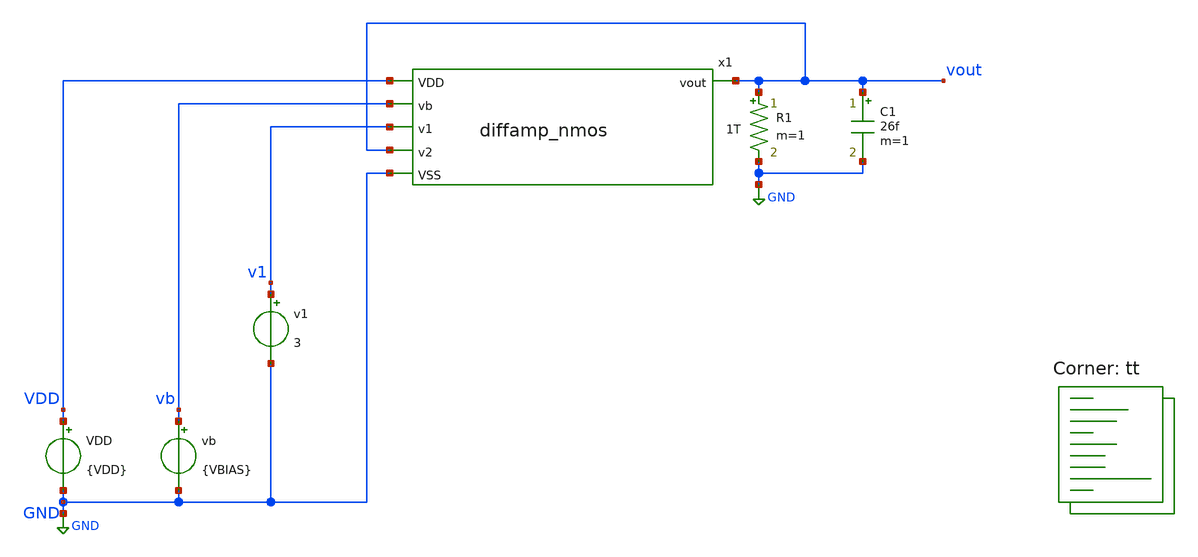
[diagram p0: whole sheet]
** sch_path: xschem/test_diffamp_nmos_load.sch
**.subckt test_diffamp_nmos_load
VDD VDD GND {VDD}
vb vb GND {VBIAS}
v1 v1 GND 3
R1 vout GND 1T m=1
x1 v1 vout GND VDD vb vout diffamp_nmos
C1 vout GND 26f m=1
**** begin user architecture code
.lib $::SKYWATER_MODELS/sky130.lib.spice tt



.options reltol=0.0001 abstol=10e-15
*.include diffamp_nmos.spice
.param VDD=6
.param VSS=0
.param VBIAS=1.2
.options savecurrents
* .options reltol=0.01 abstol=10e-12
.control
  save all
  op
  remzerovec
  write test_diffamp_nmos_load.raw
  set appendwrite
  * vb sweep
  *dc v1 0 6 0.2 vb 0 5 1
  *remzerovec
  *write test_diffamp_nmos_load.raw
  * dc sweep
  *dc v1 0 5 0.1
  *remzerovec
  *write test_diffamp_nmos_load.raw
  * Load sweep
  *dc R1 100k 10meg 100k
  dc v1 0 6 0.01 r1 100k 2meg 100k
  remzerovec
  write test_diffamp_nmos_load.raw
  * tran
  *tran 1n 3u
  *remzerovec
  *write test_diffamp_nmos_load.raw
.endc



**** end user architecture code
**.ends

* expanding   symbol:  diffamp_nmos.sym # of pins=6
** sym_path: xschem/diffamp_nmos.sym
** sch_path: xschem/diffamp_nmos.sch
.subckt diffamp_nmos v1 v2 VSS VDD vb vout
*.ipin v1
*.ipin v2
*.ipin vb
*.opin vout
*.ipin VDD
*.ipin VSS
XM7 int2 int3 VDD VDD sky130_fd_pr__pfet_g5v0d10v5 L=1 W=1.5 nf=1 ad='int((nf+1)/2) * W/nf * 0.29' as='int((nf+2)/2) * W/nf * 0.29'
+ pd='2*int((nf+1)/2) * (W/nf + 0.29)' ps='2*int((nf+2)/2) * (W/nf + 0.29)' nrd='0.29 / W' nrs='0.29 / W'
+ sa=0 sb=0 sd=0 mult=1 m=1
XM8 int2 int2 VSS VSS sky130_fd_pr__nfet_g5v0d10v5 L=1 W=1.5 nf=1 ad='int((nf+1)/2) * W/nf * 0.29' as='int((nf+2)/2) * W/nf * 0.29'
+ pd='2*int((nf+1)/2) * (W/nf + 0.29)' ps='2*int((nf+2)/2) * (W/nf + 0.29)' nrd='0.29 / W' nrs='0.29 / W'
+ sa=0 sb=0 sd=0 mult=1 m=1
XM9 vout int2 VSS VSS sky130_fd_pr__nfet_g5v0d10v5 L=1 W=1.5 nf=1 ad='int((nf+1)/2) * W/nf * 0.29' as='int((nf+2)/2) * W/nf * 0.29'
+ pd='2*int((nf+1)/2) * (W/nf + 0.29)' ps='2*int((nf+2)/2) * (W/nf + 0.29)' nrd='0.29 / W' nrs='0.29 / W'
+ sa=0 sb=0 sd=0 mult=1 m=1
XM1 int4 v1 int1 VSS sky130_fd_pr__nfet_g5v0d10v5 L=1 W=1.5 nf=1 ad='int((nf+1)/2) * W/nf * 0.29' as='int((nf+2)/2) * W/nf * 0.29'
+ pd='2*int((nf+1)/2) * (W/nf + 0.29)' ps='2*int((nf+2)/2) * (W/nf + 0.29)' nrd='0.29 / W' nrs='0.29 / W'
+ sa=0 sb=0 sd=0 mult=1 m=1
XM2 int3 v2 int1 VSS sky130_fd_pr__nfet_g5v0d10v5 L=1 W=1.5 nf=1 ad='int((nf+1)/2) * W/nf * 0.29' as='int((nf+2)/2) * W/nf * 0.29'
+ pd='2*int((nf+1)/2) * (W/nf + 0.29)' ps='2*int((nf+2)/2) * (W/nf + 0.29)' nrd='0.29 / W' nrs='0.29 / W'
+ sa=0 sb=0 sd=0 mult=1 m=1
XM6 int3 int3 VDD VDD sky130_fd_pr__pfet_g5v0d10v5 L=1 W=1.5 nf=1 ad='int((nf+1)/2) * W/nf * 0.29' as='int((nf+2)/2) * W/nf * 0.29'
+ pd='2*int((nf+1)/2) * (W/nf + 0.29)' ps='2*int((nf+2)/2) * (W/nf + 0.29)' nrd='0.29 / W' nrs='0.29 / W'
+ sa=0 sb=0 sd=0 mult=1 m=1
XM5 vout int4 VDD VDD sky130_fd_pr__pfet_g5v0d10v5 L=1 W=1.5 nf=1 ad='int((nf+1)/2) * W/nf * 0.29' as='int((nf+2)/2) * W/nf * 0.29'
+ pd='2*int((nf+1)/2) * (W/nf + 0.29)' ps='2*int((nf+2)/2) * (W/nf + 0.29)' nrd='0.29 / W' nrs='0.29 / W'
+ sa=0 sb=0 sd=0 mult=1 m=1
XM3a int1 vb int5 VSS sky130_fd_pr__nfet_g5v0d10v5 L=1 W=1.5 nf=1 ad='int((nf+1)/2) * W/nf * 0.29' as='int((nf+2)/2) * W/nf * 0.29'
+ pd='2*int((nf+1)/2) * (W/nf + 0.29)' ps='2*int((nf+2)/2) * (W/nf + 0.29)' nrd='0.29 / W' nrs='0.29 / W'
+ sa=0 sb=0 sd=0 mult=1 m=1
XM3b int5 vb VSS VSS sky130_fd_pr__nfet_g5v0d10v5 L=1 W=1.5 nf=1 ad='int((nf+1)/2) * W/nf * 0.29' as='int((nf+2)/2) * W/nf * 0.29'
+ pd='2*int((nf+1)/2) * (W/nf + 0.29)' ps='2*int((nf+2)/2) * (W/nf + 0.29)' nrd='0.29 / W' nrs='0.29 / W'
+ sa=0 sb=0 sd=0 mult=1 m=1
XM4 int4 int4 VDD VDD sky130_fd_pr__pfet_g5v0d10v5 L=1 W=1.5 nf=1 ad='int((nf+1)/2) * W/nf * 0.29' as='int((nf+2)/2) * W/nf * 0.29'
+ pd='2*int((nf+1)/2) * (W/nf + 0.29)' ps='2*int((nf+2)/2) * (W/nf + 0.29)' nrd='0.29 / W' nrs='0.29 / W'
+ sa=0 sb=0 sd=0 mult=1 m=1
.ends

.GLOBAL GND
.end
